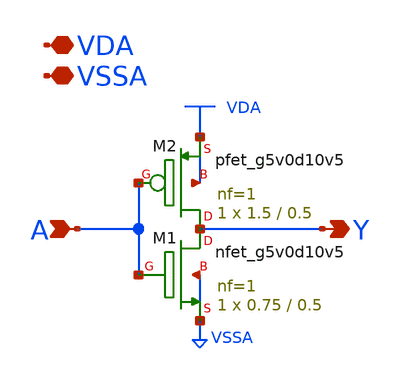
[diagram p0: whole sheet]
** sch_path: amx_inv1.sch
* Copyright 2023 David Mitchell Bailey
* Licensed under the Apache License, Version 2.0 (the "License");
* you may not use this file except in compliance with the License.
* You may obtain a copy of the License at
* https://www.apache.org/licenses/LICENSE-2.0
* Unless required by applicable law or agreed to in writing, software
* distributed under the License is distributed on an "AS IS" BASIS,
* WITHOUT WARRANTIES OR CONDITIONS OF ANY KIND, either express or implied.
* See the License for the specific language governing permissions and
* limitations under the License.
**.subckt amx_inv1 A Y VDA VSSA
*.ipin A
*.opin Y
*.iopin VDA
*.iopin VSSA
XM1 Y A VSSA VSSA sky130_fd_pr__nfet_g5v0d10v5 L=0.5 W=0.75 nf=1 ad='int((nf+1)/2) * W/nf * 0.29' as='int((nf+2)/2) * W/nf * 0.29'
+ pd='2*int((nf+1)/2) * (W/nf + 0.29)' ps='2*int((nf+2)/2) * (W/nf + 0.29)' nrd='0.29 / W' nrs='0.29 / W'
+ sa=0 sb=0 sd=0 mult=1 m=1
XM2 Y A VDA VDA sky130_fd_pr__pfet_g5v0d10v5 L=0.5 W=1.5 nf=1 ad='int((nf+1)/2) * W/nf * 0.29' as='int((nf+2)/2) * W/nf * 0.29'
+ pd='2*int((nf+1)/2) * (W/nf + 0.29)' ps='2*int((nf+2)/2) * (W/nf + 0.29)' nrd='0.29 / W' nrs='0.29 / W'
+ sa=0 sb=0 sd=0 mult=1 m=1
**.ends
.end
